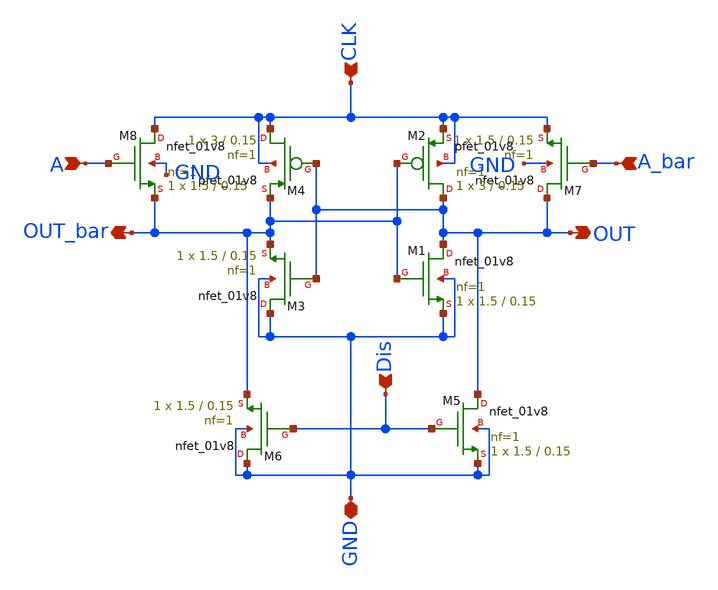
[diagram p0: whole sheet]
** sch_path: skywater_stuff/EESPFAL_INV.sch
**.subckt EESPFAL_INV A A_bar OUT_bar OUT Dis GND CLK
*.ipin A
*.ipin A_bar
*.opin OUT_bar
*.opin OUT
*.ipin Dis
*.iopin GND
*.ipin CLK
XM7 OUT A_bar CLK GND sky130_fd_pr__nfet_01v8 L=0.15 W=1.5 nf=1 ad='int((nf+1)/2) * W/nf * 0.29' as='int((nf+2)/2) * W/nf * 0.29'
+ pd='2*int((nf+1)/2) * (W/nf + 0.29)' ps='2*int((nf+2)/2) * (W/nf + 0.29)' nrd='0.29 / W' nrs='0.29 / W'
+ sa=0 sb=0 sd=0 mult=1 m=1
XM3 GND OUT OUT_bar GND sky130_fd_pr__nfet_01v8 L=0.15 W=1.5 nf=1 ad='int((nf+1)/2) * W/nf * 0.29' as='int((nf+2)/2) * W/nf * 0.29'
+ pd='2*int((nf+1)/2) * (W/nf + 0.29)' ps='2*int((nf+2)/2) * (W/nf + 0.29)' nrd='0.29 / W' nrs='0.29 / W'
+ sa=0 sb=0 sd=0 mult=1 m=1
XM5 OUT Dis GND GND sky130_fd_pr__nfet_01v8 L=0.15 W=1.5 nf=1 ad='int((nf+1)/2) * W/nf * 0.29' as='int((nf+2)/2) * W/nf * 0.29'
+ pd='2*int((nf+1)/2) * (W/nf + 0.29)' ps='2*int((nf+2)/2) * (W/nf + 0.29)' nrd='0.29 / W' nrs='0.29 / W'
+ sa=0 sb=0 sd=0 mult=1 m=1
XM6 GND Dis OUT_bar GND sky130_fd_pr__nfet_01v8 L=0.15 W=1.5 nf=1 ad='int((nf+1)/2) * W/nf * 0.29' as='int((nf+2)/2) * W/nf * 0.29'
+ pd='2*int((nf+1)/2) * (W/nf + 0.29)' ps='2*int((nf+2)/2) * (W/nf + 0.29)' nrd='0.29 / W' nrs='0.29 / W'
+ sa=0 sb=0 sd=0 mult=1 m=1
XM8 CLK A OUT_bar GND sky130_fd_pr__nfet_01v8 L=0.15 W=1.5 nf=1 ad='int((nf+1)/2) * W/nf * 0.29' as='int((nf+2)/2) * W/nf * 0.29'
+ pd='2*int((nf+1)/2) * (W/nf + 0.29)' ps='2*int((nf+2)/2) * (W/nf + 0.29)' nrd='0.29 / W' nrs='0.29 / W'
+ sa=0 sb=0 sd=0 mult=1 m=1
XM2 OUT OUT_bar CLK CLK sky130_fd_pr__pfet_01v8 L=0.15 W=3 nf=1 ad='int((nf+1)/2) * W/nf * 0.29' as='int((nf+2)/2) * W/nf * 0.29'
+ pd='2*int((nf+1)/2) * (W/nf + 0.29)' ps='2*int((nf+2)/2) * (W/nf + 0.29)' nrd='0.29 / W' nrs='0.29 / W'
+ sa=0 sb=0 sd=0 mult=1 m=1
XM1 OUT OUT_bar GND GND sky130_fd_pr__nfet_01v8 L=0.15 W=1.5 nf=1 ad='int((nf+1)/2) * W/nf * 0.29' as='int((nf+2)/2) * W/nf * 0.29'
+ pd='2*int((nf+1)/2) * (W/nf + 0.29)' ps='2*int((nf+2)/2) * (W/nf + 0.29)' nrd='0.29 / W' nrs='0.29 / W'
+ sa=0 sb=0 sd=0 mult=1 m=1
XM4 CLK OUT OUT_bar CLK sky130_fd_pr__pfet_01v8 L=0.15 W=3 nf=1 ad='int((nf+1)/2) * W/nf * 0.29' as='int((nf+2)/2) * W/nf * 0.29'
+ pd='2*int((nf+1)/2) * (W/nf + 0.29)' ps='2*int((nf+2)/2) * (W/nf + 0.29)' nrd='0.29 / W' nrs='0.29 / W'
+ sa=0 sb=0 sd=0 mult=1 m=1
**.ends
.end
